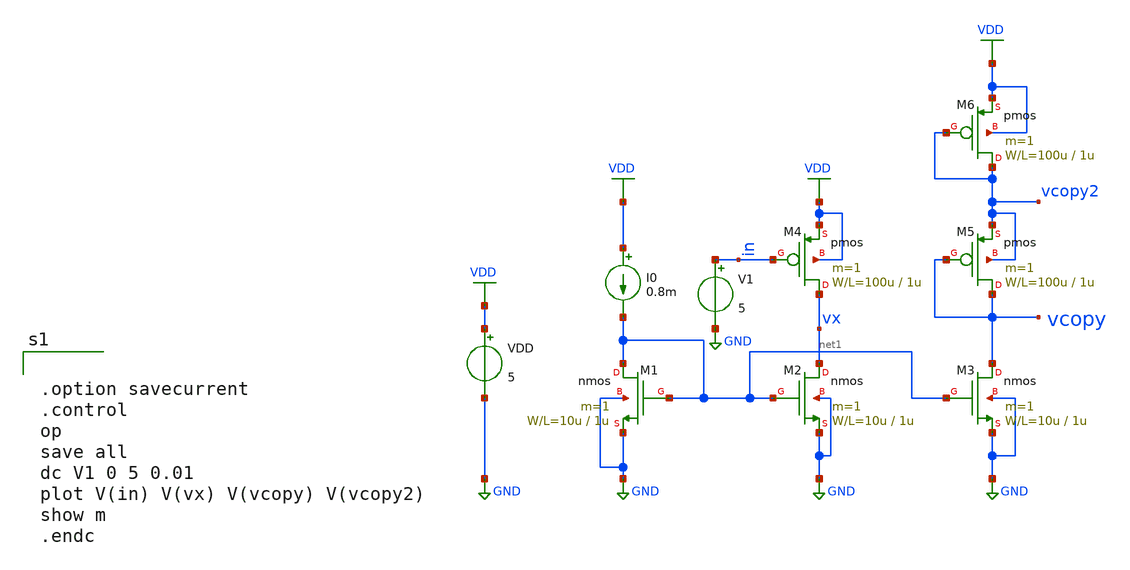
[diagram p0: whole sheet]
** sch_path: member_project/GroupWork/Team_masahiro/bias_replica_2.sch
**.subckt bias_replica_2
M1 net1 net1 GND GND nmos L=1u W=10u m=1
I0 VDD net1 0.8m
M2 vx net1 GND GND nmos L=1u W=10u m=1
VDD VDD GND 5
M3 vcopy net1 GND GND nmos L=1u W=10u m=1
M4 vx in VDD VDD pmos L=1u W=100u m=1
M5 vcopy vcopy vcopy2 vcopy2 pmos L=1u W=100u m=1
V1 in GND 5
M6 vcopy2 vcopy2 VDD VDD pmos L=1u W=100u m=1
**** begin user architecture code
 .include $::LIB/mos.lib
.include $::LIB/passive.lib
.include $::LIB/diode.lib


.option savecurrent
.control
op
save all
dc V1 0 5 0.01
plot V(in) V(vx) V(vcopy) V(vcopy2)
show m
.endc


**** end user architecture code
**.ends
.GLOBAL GND
.GLOBAL VDD
.end
